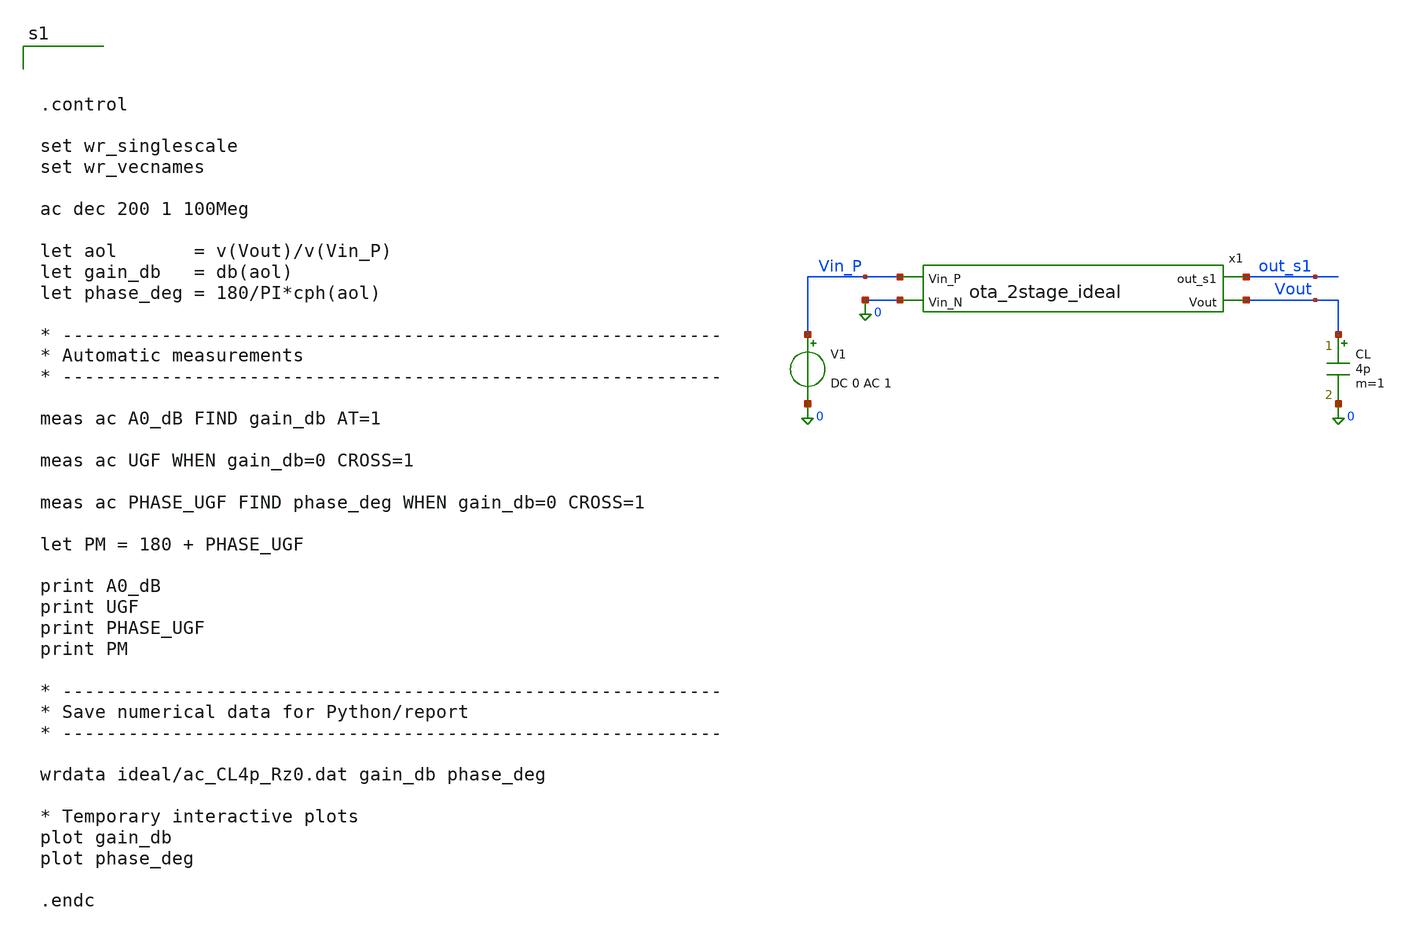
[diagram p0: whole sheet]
** sch_path: dfii/project_2stage_OTA_sim/tb_ota_2stage_ideal_ac.sch
**.subckt tb_ota_2stage_ideal_ac
x1 out_s1 Vout Vin_P 0 ota_2stage_ideal
CL Vout 0 4p m=1
V1 Vin_P 0 DC 0 AC 1
**** begin user architecture code



.control

set wr_singlescale
set wr_vecnames

ac dec 200 1 100Meg

let aol       = v(Vout)/v(Vin_P)
let gain_db   = db(aol)
let phase_deg = 180/PI*cph(aol)

* ------------------------------------------------------------
* Automatic measurements
* ------------------------------------------------------------

meas ac A0_dB FIND gain_db AT=1

meas ac UGF WHEN gain_db=0 CROSS=1

meas ac PHASE_UGF FIND phase_deg WHEN gain_db=0 CROSS=1

let PM = 180 + PHASE_UGF

print A0_dB
print UGF
print PHASE_UGF
print PM

* ------------------------------------------------------------
* Save numerical data for Python/report
* ------------------------------------------------------------

wrdata ideal/ac_CL4p_Rz0.dat gain_db phase_deg

* Temporary interactive plots
plot gain_db
plot phase_deg

.endc


**** end user architecture code
**.ends

* expanding   symbol:  /foss/designs/project_2stage_OTA/dfii/project_2stage_OTA/ota_2stage_ideal.sym
*+ # of pins=4
** sym_path: dfii/project_2stage_OTA/ota_2stage_ideal.sym
** sch_path: dfii/project_2stage_OTA/ota_2stage_ideal.sch
.subckt ota_2stage_ideal out_s1 Vout Vin_P Vin_N
*.ipin Vin_P
*.ipin Vin_N
*.opin out_s1
*.opin Vout
G_STAGE1 out_s1 0 Vin_P Vin_N 5u
G_STAGE2 Vout 0 out_s1 0 54.4u
ROUT_S1 out_s1 0 29.7Meg m=1
ROUT_S2 Vout 0 2.81Meg m=1
CMILLER out_s1 net1 0.8p m=1
RMILLER net1 Vout 110k m=1
.ends

.end
